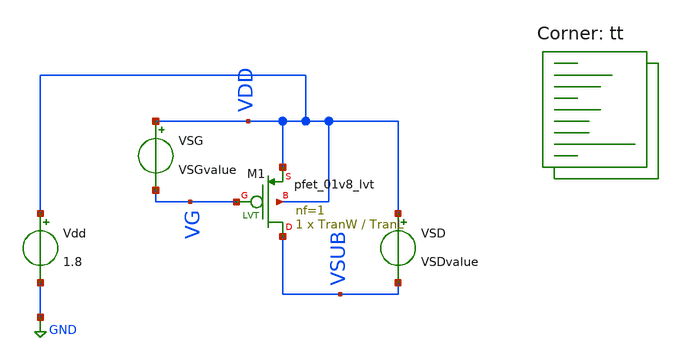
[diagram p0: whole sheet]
** sch_path: Schematics/PMOSlvtchar.sch
**.subckt PMOSlvtchar
Vdd VDD GND 1.8
VSD VDD VSUB VSDvalue
VSG VDD VG VSGvalue
XM1 VSUB VG VDD VDD sky130_fd_pr__pfet_01v8_lvt L=TranL W=TranW nf=1 ad='int((nf+1)/2) * W/nf * 0.29'
+ as='int((nf+2)/2) * W/nf * 0.29' pd='2*int((nf+1)/2) * (W/nf + 0.29)' ps='2*int((nf+2)/2) * (W/nf + 0.29)'
+ nrd='0.29 / W' nrs='0.29 / W' sa=0 sb=0 sd=0 mult=1 m=1
**** begin user architecture code
.lib $::SKYWATER_MODELS/sky130.lib.spice tt
**** end user architecture code
**.ends
.GLOBAL GND
.end
